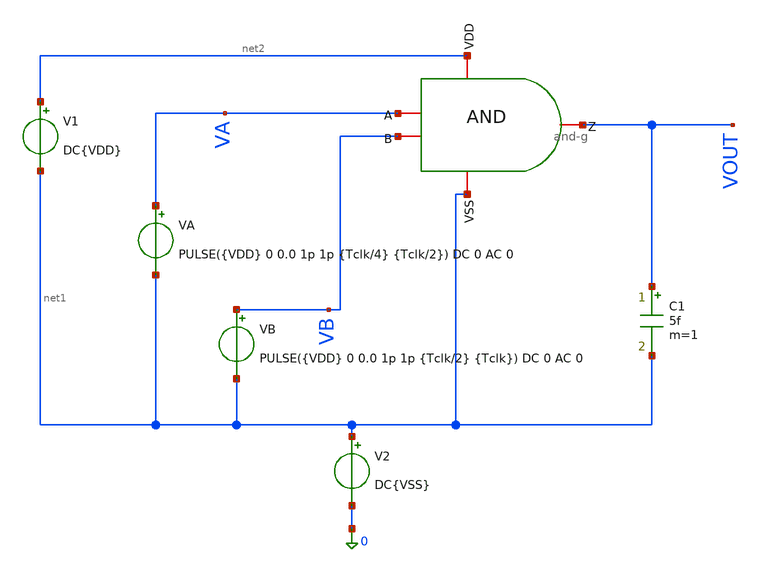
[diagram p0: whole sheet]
** sch_path: verification/testbenches/tb_and-g.sch
**.subckt tb_and-g
VA VA net1 PULSE({VDD} 0 0.0 1p 1p {Tclk/4} {Tclk/2}) DC 0 AC 0
V1 net2 net1 DC{VDD}
VB VB net1 PULSE({VDD} 0 0.0 1p 1p {Tclk/2} {Tclk}) DC 0 AC 0
V2 net1 0 DC{VSS}
C1 VOUT net1 5f m=1
x1 net2 VA VB VOUT net1 and-g
**** begin user architecture code


* Circuit Parameters
.param VDD = 1.2
.param VSS = 0.0
.param Tclk = 10n
.options TEMP = 27.0
* Include Models - IHP SG13G2
.lib cornerMOSlv.lib mos_tt
* OP Parameters & Singals to save
.save all
*Simulations
.control
tran 0.01u 100n
setplot tran1
plot v(VA) v(VB)+1.5 v(VOUT)+3
set filetype = ascii
write dcsweep.raw
.endc
.end


**** end user architecture code
**.ends
.end
